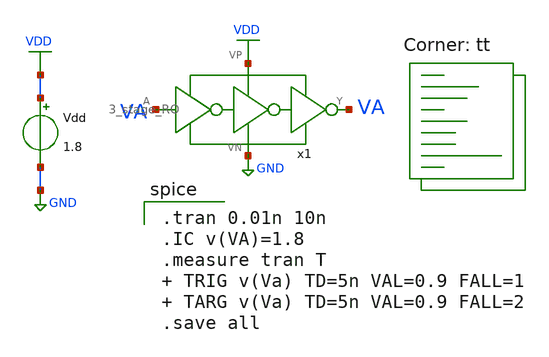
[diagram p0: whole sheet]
** sch_path: week 4/sim/5/RO_test.sch
**.subckt RO_test
Vdd VDD GND 1.8
x1 VA VDD VA GND 3_stage_RO
**** begin user architecture code

.tran 0.01n 10n
.IC v(VA)=1.8
.measure tran T  TRIG v(Va) TD=5n VAL=0.9 FALL=1  TARG v(Va) TD=5n VAL=0.9 FALL=2
.save all

 .lib /usr/local/share/pdk/sky130A/libs.tech/ngspice/sky130.lib.spice tt
**** end user architecture code
**.ends

* expanding   symbol:  VSD/week3/(0)pre-layout-ring/3_stage_RO.sym # of pins=4
** sym_path: week 3/sim/1/3_stage_RO.sym
** sch_path: week 3/sim/1/3_stage_RO.sch
.subckt 3_stage_RO A VP Y VN
*.ipin A
*.opin Y
*.iopin VN
*.iopin VP
XM1 net1 A VN VN sky130_fd_pr__nfet_01v8 L=0.15 W=0.42 nf=2 ad='int((nf+1)/2) * W/nf * 0.29' as='int((nf+2)/2) * W/nf * 0.29'
+ pd='2*int((nf+1)/2) * (W/nf + 0.29)' ps='2*int((nf+2)/2) * (W/nf + 0.29)' nrd='0.29 / W' nrs='0.29 / W'
+ sa=0 sb=0 sd=0 mult=1 m=1
XM2 net1 A VP VP sky130_fd_pr__pfet_01v8 L=0.15 W=0.42 nf=2 ad='int((nf+1)/2) * W/nf * 0.29' as='int((nf+2)/2) * W/nf * 0.29'
+ pd='2*int((nf+1)/2) * (W/nf + 0.29)' ps='2*int((nf+2)/2) * (W/nf + 0.29)' nrd='0.29 / W' nrs='0.29 / W'
+ sa=0 sb=0 sd=0 mult=1 m=1
XM3 net2 net1 VN VN sky130_fd_pr__nfet_01v8 L=0.15 W=0.42 nf=2 ad='int((nf+1)/2) * W/nf * 0.29' as='int((nf+2)/2) * W/nf * 0.29'
+ pd='2*int((nf+1)/2) * (W/nf + 0.29)' ps='2*int((nf+2)/2) * (W/nf + 0.29)' nrd='0.29 / W' nrs='0.29 / W'
+ sa=0 sb=0 sd=0 mult=1 m=1
XM4 net2 net1 VP VP sky130_fd_pr__pfet_01v8 L=0.15 W=0.42 nf=2 ad='int((nf+1)/2) * W/nf * 0.29' as='int((nf+2)/2) * W/nf * 0.29'
+ pd='2*int((nf+1)/2) * (W/nf + 0.29)' ps='2*int((nf+2)/2) * (W/nf + 0.29)' nrd='0.29 / W' nrs='0.29 / W'
+ sa=0 sb=0 sd=0 mult=1 m=1
XM5 Y net2 VN VN sky130_fd_pr__nfet_01v8 L=0.15 W=0.42 nf=2 ad='int((nf+1)/2) * W/nf * 0.29' as='int((nf+2)/2) * W/nf * 0.29'
+ pd='2*int((nf+1)/2) * (W/nf + 0.29)' ps='2*int((nf+2)/2) * (W/nf + 0.29)' nrd='0.29 / W' nrs='0.29 / W'
+ sa=0 sb=0 sd=0 mult=1 m=1
XM6 Y net2 VP VP sky130_fd_pr__pfet_01v8 L=0.15 W=0.42 nf=2 ad='int((nf+1)/2) * W/nf * 0.29' as='int((nf+2)/2) * W/nf * 0.29'
+ pd='2*int((nf+1)/2) * (W/nf + 0.29)' ps='2*int((nf+2)/2) * (W/nf + 0.29)' nrd='0.29 / W' nrs='0.29 / W'
+ sa=0 sb=0 sd=0 mult=1 m=1
.ends

.GLOBAL VDD
.GLOBAL GND
.end
